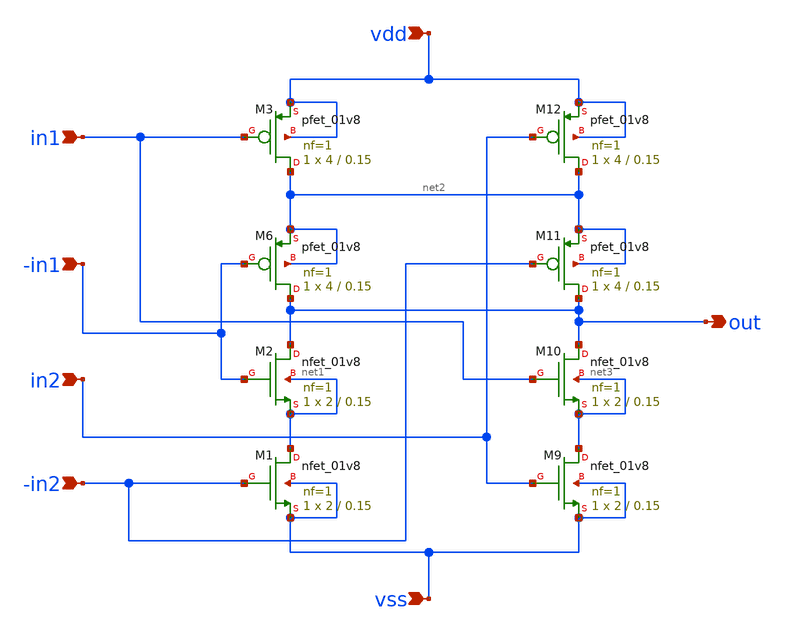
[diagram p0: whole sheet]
** sch_path: projects/carry_lookahead_adder/xschem/ports/_xor.sch
**.subckt _xor in1 -in1 vdd vss out in2 -in2
*.ipin in1
*.ipin -in1
*.ipin vdd
*.ipin vss
*.opin out
*.ipin in2
*.ipin -in2
XM1 net1 -in2 vss vss sky130_fd_pr__nfet_01v8 L=0.15 W=2 nf=1 ad='int((nf+1)/2) * W/nf * 0.29' as='int((nf+2)/2) * W/nf * 0.29'
+ pd='2*int((nf+1)/2) * (W/nf + 0.29)' ps='2*int((nf+2)/2) * (W/nf + 0.29)' nrd='0.29 / W' nrs='0.29 / W'
+ sa=0 sb=0 sd=0 mult=1 m=1
XM2 out -in1 net1 net1 sky130_fd_pr__nfet_01v8 L=0.15 W=2 nf=1 ad='int((nf+1)/2) * W/nf * 0.29' as='int((nf+2)/2) * W/nf * 0.29'
+ pd='2*int((nf+1)/2) * (W/nf + 0.29)' ps='2*int((nf+2)/2) * (W/nf + 0.29)' nrd='0.29 / W' nrs='0.29 / W'
+ sa=0 sb=0 sd=0 mult=1 m=1
XM6 out -in1 net2 net2 sky130_fd_pr__pfet_01v8 L=0.15 W=4 nf=1 ad='int((nf+1)/2) * W/nf * 0.29' as='int((nf+2)/2) * W/nf * 0.29'
+ pd='2*int((nf+1)/2) * (W/nf + 0.29)' ps='2*int((nf+2)/2) * (W/nf + 0.29)' nrd='0.29 / W' nrs='0.29 / W'
+ sa=0 sb=0 sd=0 mult=1 m=1
XM3 net2 in1 vdd vdd sky130_fd_pr__pfet_01v8 L=0.15 W=4 nf=1 ad='int((nf+1)/2) * W/nf * 0.29' as='int((nf+2)/2) * W/nf * 0.29'
+ pd='2*int((nf+1)/2) * (W/nf + 0.29)' ps='2*int((nf+2)/2) * (W/nf + 0.29)' nrd='0.29 / W' nrs='0.29 / W'
+ sa=0 sb=0 sd=0 mult=1 m=1
XM9 net3 in2 vss vss sky130_fd_pr__nfet_01v8 L=0.15 W=2 nf=1 ad='int((nf+1)/2) * W/nf * 0.29' as='int((nf+2)/2) * W/nf * 0.29'
+ pd='2*int((nf+1)/2) * (W/nf + 0.29)' ps='2*int((nf+2)/2) * (W/nf + 0.29)' nrd='0.29 / W' nrs='0.29 / W'
+ sa=0 sb=0 sd=0 mult=1 m=1
XM10 out in1 net3 net3 sky130_fd_pr__nfet_01v8 L=0.15 W=2 nf=1 ad='int((nf+1)/2) * W/nf * 0.29' as='int((nf+2)/2) * W/nf * 0.29'
+ pd='2*int((nf+1)/2) * (W/nf + 0.29)' ps='2*int((nf+2)/2) * (W/nf + 0.29)' nrd='0.29 / W' nrs='0.29 / W'
+ sa=0 sb=0 sd=0 mult=1 m=1
XM11 out -in2 net2 net2 sky130_fd_pr__pfet_01v8 L=0.15 W=4 nf=1 ad='int((nf+1)/2) * W/nf * 0.29' as='int((nf+2)/2) * W/nf * 0.29'
+ pd='2*int((nf+1)/2) * (W/nf + 0.29)' ps='2*int((nf+2)/2) * (W/nf + 0.29)' nrd='0.29 / W' nrs='0.29 / W'
+ sa=0 sb=0 sd=0 mult=1 m=1
XM12 net2 in2 vdd vdd sky130_fd_pr__pfet_01v8 L=0.15 W=4 nf=1 ad='int((nf+1)/2) * W/nf * 0.29' as='int((nf+2)/2) * W/nf * 0.29'
+ pd='2*int((nf+1)/2) * (W/nf + 0.29)' ps='2*int((nf+2)/2) * (W/nf + 0.29)' nrd='0.29 / W' nrs='0.29 / W'
+ sa=0 sb=0 sd=0 mult=1 m=1
**.ends
.end
